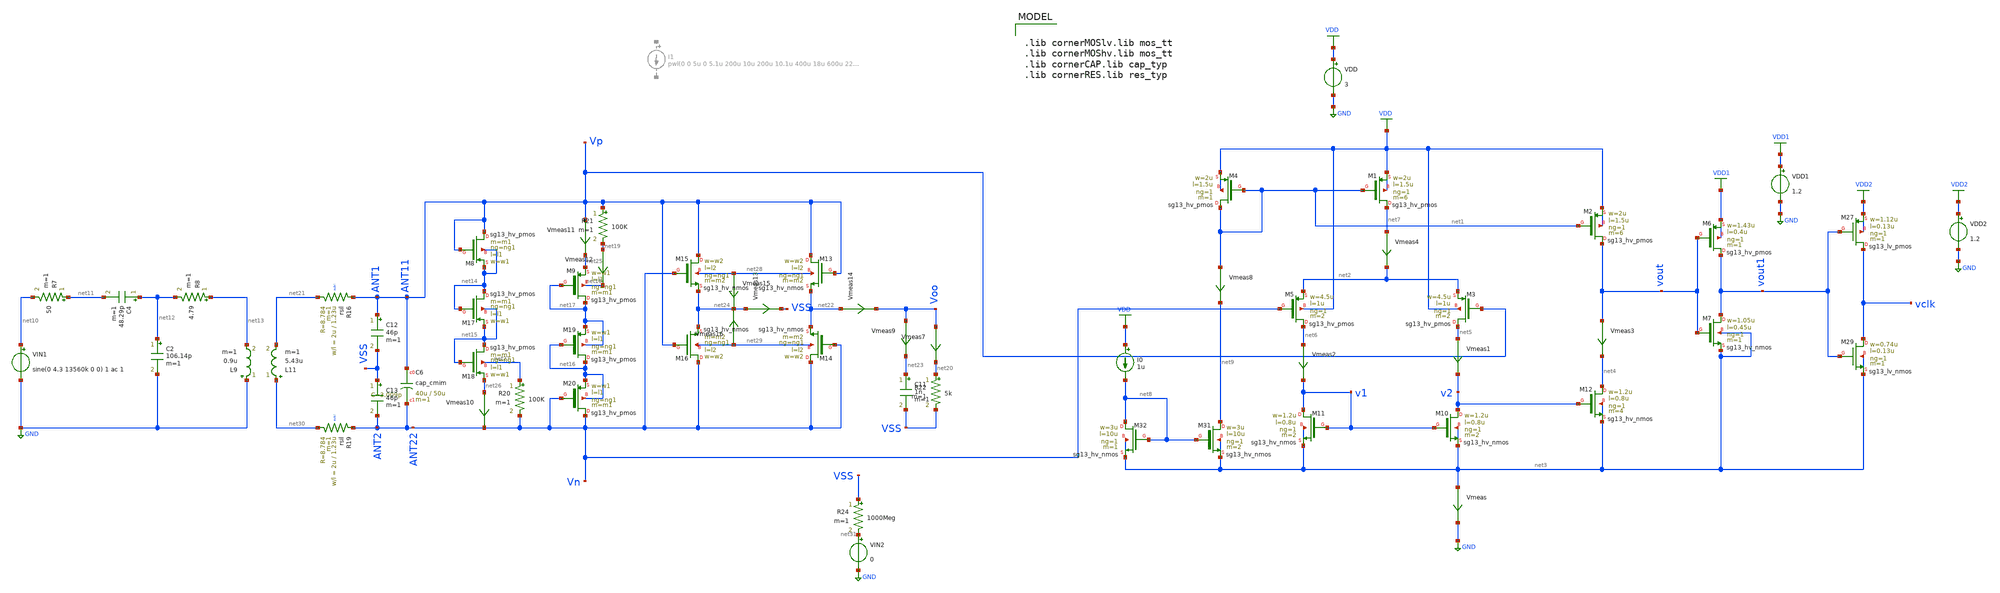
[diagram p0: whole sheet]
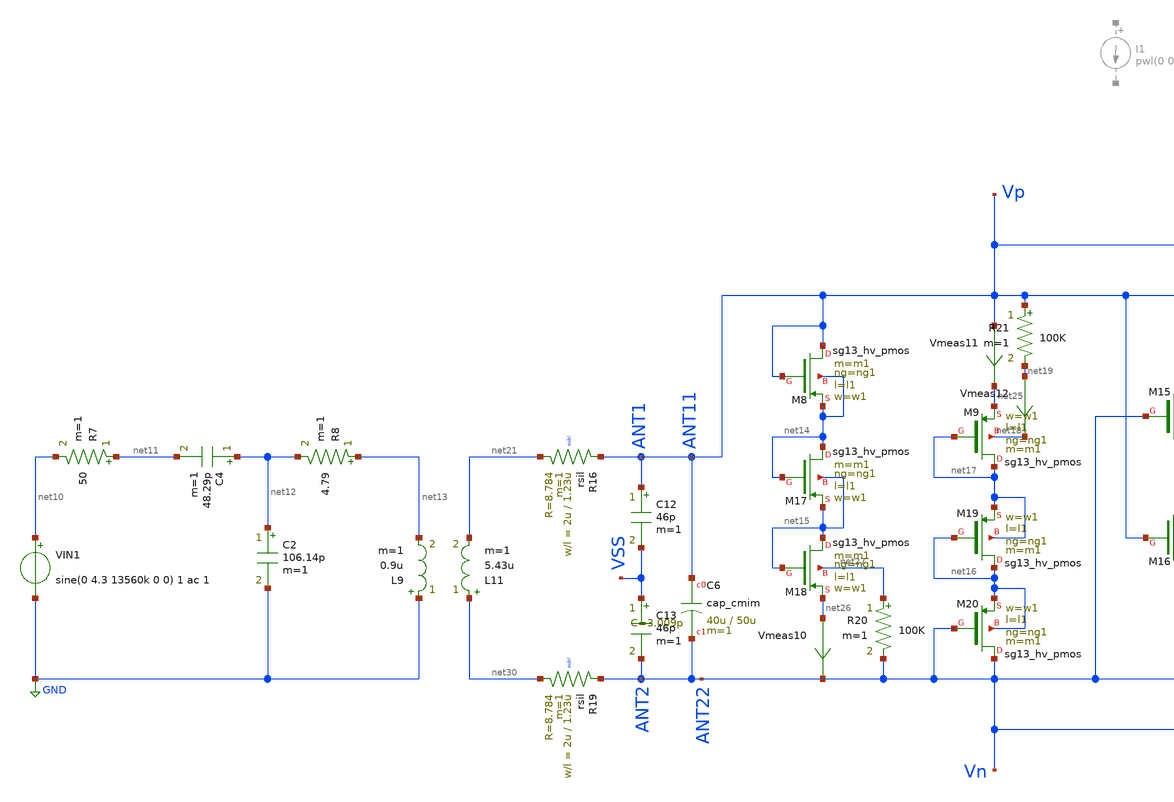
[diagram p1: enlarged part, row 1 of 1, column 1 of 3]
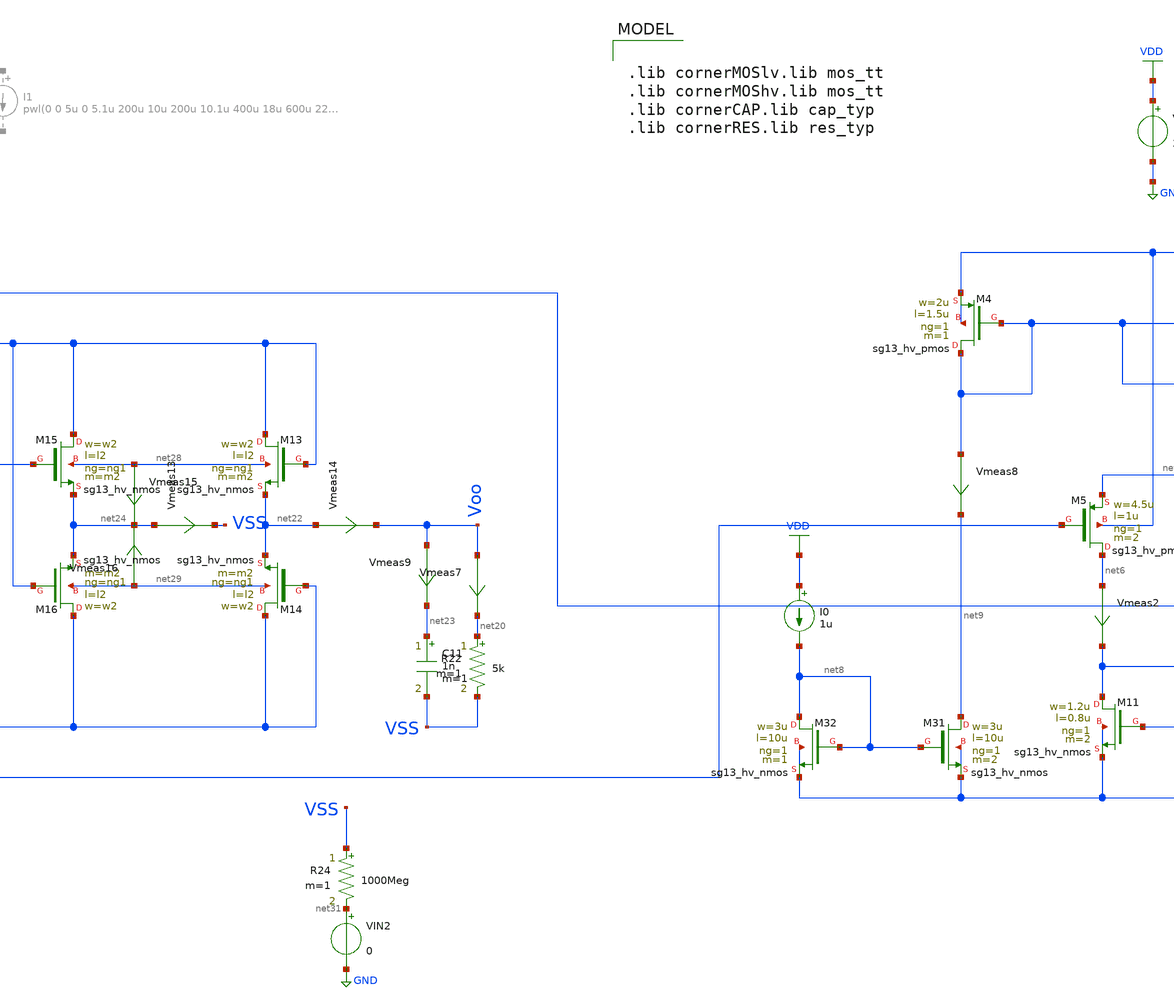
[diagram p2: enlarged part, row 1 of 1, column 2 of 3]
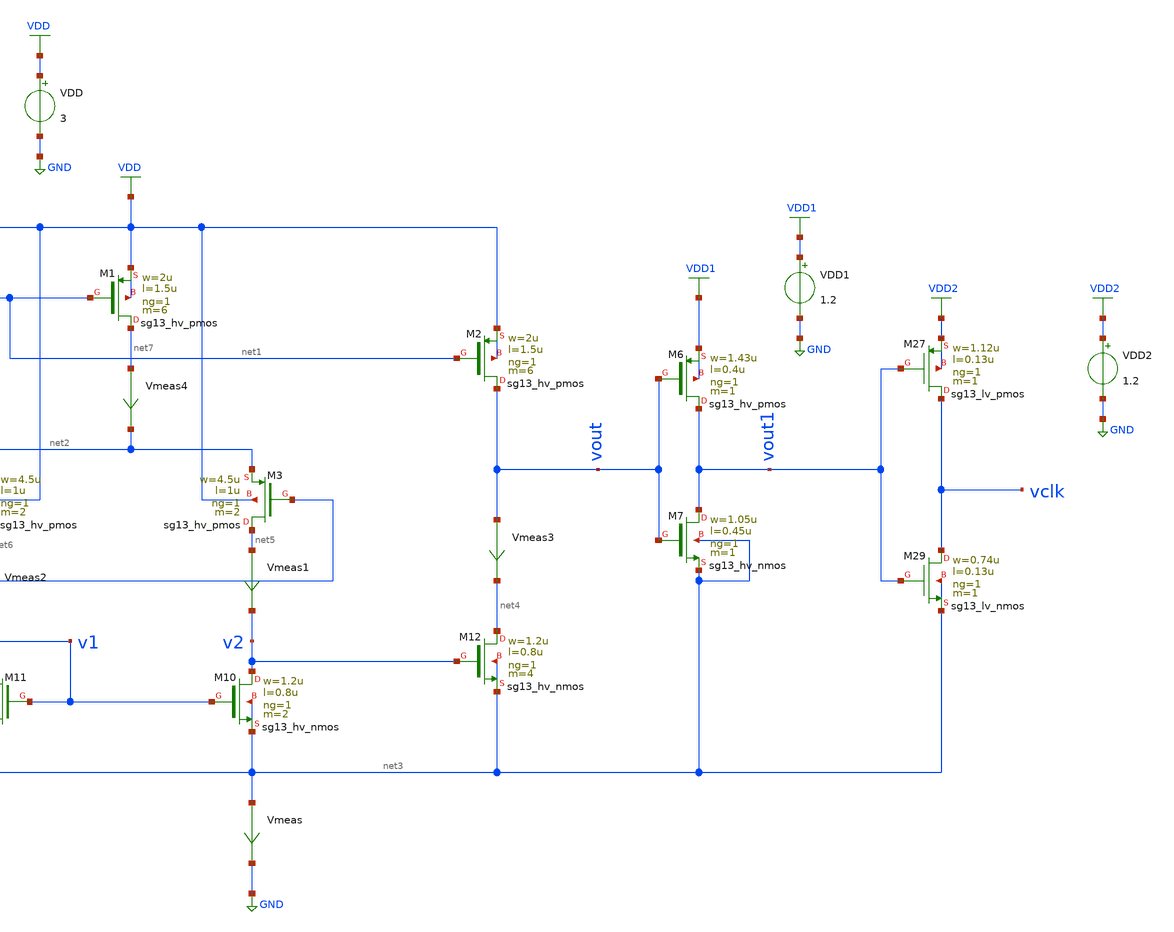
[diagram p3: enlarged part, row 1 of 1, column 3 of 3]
** sch_path: dependencies/ClockExtractor/ClockExtractor-main/testbenches/tran/xschem/clock_extractor_tran_2026 .sch
**.subckt clock_extractor_tran_2026
VDD VDD GND 3
VDD1 VDD1 GND 1.2
XM7 vout1 vout net3 net3 sg13_hv_nmos w=1.05u l=0.45u ng=1 m=1 mm_ok=1
XM6 vout1 vout VDD1 VDD1 sg13_hv_pmos w=1.43u l=0.4u ng=1 m=1 mm_ok=1
XM4 net1 net1 VDD VDD sg13_hv_pmos w=2u l=1.5u ng=1 m=1 mm_ok=1
XM1 net7 net1 VDD VDD sg13_hv_pmos w=2u l=1.5u ng=1 m=6 mm_ok=1
XM2 vout net1 VDD VDD sg13_hv_pmos w=2u l=1.5u ng=1 m=6 mm_ok=1
XM3 net5 ANT11 net2 VDD sg13_hv_pmos w=4.5u l=1u ng=1 m=2 mm_ok=1
XM5 net6 ANT22 net2 VDD sg13_hv_pmos w=4.5u l=1u ng=1 m=2 mm_ok=1
XM10 v2 v1 net3 net3 sg13_hv_nmos w=1.2u l=0.8u ng=1 m=2 mm_ok=1
XM11 v1 v1 net3 net3 sg13_hv_nmos w=1.2u l=0.8u ng=1 m=2 mm_ok=1
XM12 net4 v2 net3 net3 sg13_hv_nmos w=1.2u l=0.8u ng=1 m=4 mm_ok=1
Vmeas net3 GND 0
.save i(vmeas)
Vmeas1 net5 v2 0
.save i(vmeas1)
Vmeas2 net6 v1 0
.save i(vmeas2)
Vmeas3 vout net4 0
.save i(vmeas3)
Vmeas4 net7 net2 0
.save i(vmeas4)
XM27 vclk vout1 VDD2 VDD2 sg13_lv_pmos w=1.12u l=0.13u ng=1 m=1 mm_ok=1
XM29 vclk vout1 net3 net3 sg13_lv_nmos w=0.74u l=0.13u ng=1 m=1 mm_ok=1
VDD2 VDD2 GND 1.2
XM31 net9 net8 net3 net3 sg13_hv_nmos w=3u l=10u ng=1 m=2 mm_ok=1
XM32 net8 net8 net3 net3 sg13_hv_nmos w=3u l=10u ng=1 m=1 mm_ok=1
Vmeas8 net1 net9 0
.save i(vmeas8)
I0 VDD net8 1u
VIN1 net10 GND sine(0 4.3 13560k 0 0) 1 ac 1

L9 GND net13 0.9u m=1
C2 net12 GND 106.14p m=1
R7 net11 net10 50 m=1
C4 net12 net11 48.29p m=1
R8 net13 net12 4.79 m=1
L11 net30 net21 5.43u m=1
XR16 ANT11 net21 sub! rsil w=2u l=1.23u m=1 mm_ok=1
XR19 ANT22 net30 sub! rsil w=2u l=1.23u m=1 mm_ok=1
XC6 ANT11 ANT22 cap_cmim w=40u l=50u m=1 mm_ok=1
XM8 ANT11 ANT11 net14 net14 sg13_hv_pmos w=w1 l=l1 ng=ng1 m=m1 mm_ok=1
XM9 net17 net17 net25 net18 sg13_hv_pmos w=w1 l=l1 ng=ng1 m=m1 mm_ok=1
R20 net27 ANT22 100K m=1
R21 ANT11 net19 100K m=1
XM13 ANT11 ANT11 net22 net28 sg13_hv_nmos w=w2 l=l2 ng=ng1 m=m2 mm_ok=1
XM14 ANT22 ANT22 net22 net29 sg13_hv_nmos w=w2 l=l2 ng=ng1 m=m2 mm_ok=1
C11 net23 VSS 1n m=1
R22 net20 VSS 5k m=1
Vmeas12 net19 net18 0
.save i(vmeas12)
C12 ANT11 VSS 46p m=1
C13 VSS ANT22 46p m=1
XM15 ANT11 ANT22 net24 net28 sg13_hv_nmos w=w2 l=l2 ng=ng1 m=m2 mm_ok=1
XM16 ANT22 ANT11 net24 net29 sg13_hv_nmos w=w2 l=l2 ng=ng1 m=m2 mm_ok=1
XM17 net14 net14 net15 net15 sg13_hv_pmos w=w1 l=l1 ng=ng1 m=m1 mm_ok=1
XM18 net15 net15 net26 net27 sg13_hv_pmos w=w1 l=l1 ng=ng1 m=m1 mm_ok=1
XM19 net16 net16 net17 net17 sg13_hv_pmos w=w1 l=l1 ng=ng1 m=m1 mm_ok=1
XM20 ANT22 ANT22 net16 net16 sg13_hv_pmos w=w1 l=l1 ng=ng1 m=m1 mm_ok=1
Vmeas7 Voo net20 0
.save i(vmeas7)
Vmeas9 Voo net23 0
.save i(vmeas9)
Vmeas10 net26 ANT22 0
.save i(vmeas10)
Vmeas11 ANT11 net25 0
.save i(vmeas11)
Vmeas13 net24 VSS 0
.save i(vmeas13)
Vmeas14 net22 Voo 0
.save i(vmeas14)
Vmeas15 net28 net24 0
.save i(vmeas15)
Vmeas16 net29 net24 0
.save i(vmeas16)
R24 VSS net31 1000Meg m=1
VIN2 net31 GND 0
**** begin user architecture code

.lib cornerMOSlv.lib mos_tt
.lib cornerMOShv.lib mos_tt
.lib cornerCAP.lib cap_typ
.lib cornerRES.lib res_typ



.param temp=27
.options rshunt =1e12
.param w1=5u
.param w2=10u
.param l1=0.5u
.param l2=1u
.param ng1=1
.param m1=20
.param m2=10
.param Coef=0.1
.save all
.control
 save all
* Transient simulation
op
tran 50p 12u
plot vclk
//plot vout
//plot vout1
plot i(Vmeas7)
plot i(Vmeas)
//plot vout2
plot Vp-Vn

meas tran avg_current AVG I(VDD)  from=5u to=5.5u
let  power_VDD=3*avg_current
meas tran avg_current_1 AVG I(VDD1) from=5u to=5.5u
let  power_VDD1=1.2*avg_current_1
meas tran avg_current_2 AVG I(VDD2) from=5u to=5.5u
let  power_VDD2=1.2*avg_current_2
let total_power=power_VDD + power_VDD1 + power_VDD2

meas tran thigh TRIG v(vclk) VAL=1.08 RISE=39 TARG v(vclk) VAL=1.08 FALL=39
meas tran tlow TRIG  v(vclk)  VAL=0.12 FALL=39  TARG v(vclk) VAL=0.12 RISE=40

//meas tran thigh TRIG v(vclk) VAl=0.6 RISE=25 TARG v(vclk) VAl=0.6 FALL=25
//meas tran tlow  TRIG v(vclk) VAl=0.6 FALL=25 TARG v(vclk) VAl=0.6 RISE=26
  * rise time and fall time
meas tran t100 when v(vclk)=0.12 rise=25
meas tran t90  when  v(vclk)=1.08 rise=25

let RiseTime = t90 - t100

meas tran t90_f when v(vclk)=1.08 fall=25
meas tran t10_f when v(vclk)=0.12 fall=25

let FallTime = t10_f - t90_f

meas tran t1 when v(vclk)=0.6 rise=25
meas tran t2 when v(vclk)=0.6 rise=26
let period1 =(t2 - t1)
let freq1 =1/period1

meas tran t3 when v(vclk)=0.6 rise=27
let period2 =(t3 - t2)
let freq2 =1/period2

meas tran t4 when v(vclk)=0.6 rise=28
let period3 =(t4 - t3)
let freq3 =1/period3

meas tran t5 when v(vclk)=0.6 rise=29
let period4 =(t5 - t4)
let freq4 =1/period4

meas tran t6 when v(vclk)=0.6 rise=30
let period5 =(t6 - t5)
let freq5 =1/period5


meas tran t7 when v(vclk)=0.6 rise=31
let period6 =(t7 - t6)
let freq6 =1/period6

meas tran t8 when v(vclk)=0.6 rise=32
let period7 =(t8 - t7)
let freq7 =1/period7

meas tran t9 when v(vclk)=0.6 rise=33
let period8 =(t9 - t8)
let freq8 =1/period8

meas tran t10 when v(vclk)=0.6 rise=34
let period9 =(t10 - t9)
let freq9 =1/period9

meas tran t11 when v(vclk)=0.6 rise=35
let period10 =(t11 - t10)
let freq10 =1/period10


meas tran t12 when v(vclk)=0.6 rise=36
let period11 =(t12 - t11)
let freq11 =1/period11

meas tran t13 when v(vclk)=0.6 rise=37
let period12 =(t13 - t12)
let freq12 =1/period12

meas tran t14 when v(vclk)=0.6 rise=38
let period13 =(t14 - t13)
let freq13 =1/period13

meas tran t15 when v(vclk)=0.6 rise=39
let period14 =(t15 - t14)
let freq14 =1/period14

meas tran t16 when v(vclk)=0.6 rise=40
let period15 =(t16 - t15)
let freq15 =1/period15


meas tran t17 when v(vclk)=0.6 rise=41
let period16 =(t17 - t16)
let freq16 =1/period16

meas tran t18 when v(vclk)=0.6 rise=42
let period17 =(t18 - t17)
let freq17 =1/period17

meas tran t19 when v(vclk)=0.6 rise=43
let period18 =(t19 - t18)
let freq18 =1/period18


meas tran t20 when v(vclk)=0.6 rise=44
let period19 =(t20 - t19)
let freq19 =1/period19

meas tran t21 when v(vclk)=0.6 rise=54
let period20 =(t21 - t20)/10
let freq20 =1/period20


let duty_cycle =thigh/(period1)*100


print freq1
print freq2
print freq3
print freq4
print freq5
print freq6
print freq7
print freq8
print freq9
print freq10
print freq11
print freq12
print freq13
print freq14
print freq15
print freq16
print freq17
print freq18
print freq19
print freq20

print thigh
print tlow
print RiseTime
print FallTime
print duty_cycle
print total_power


 write clock_extractor_10mars2026.raw
.endc
K1 L9 L11  0.7


**** end user architecture code
**.ends
.GLOBAL GND
.GLOBAL VDD
.GLOBAL VDD1
.GLOBAL VDD2
.end
